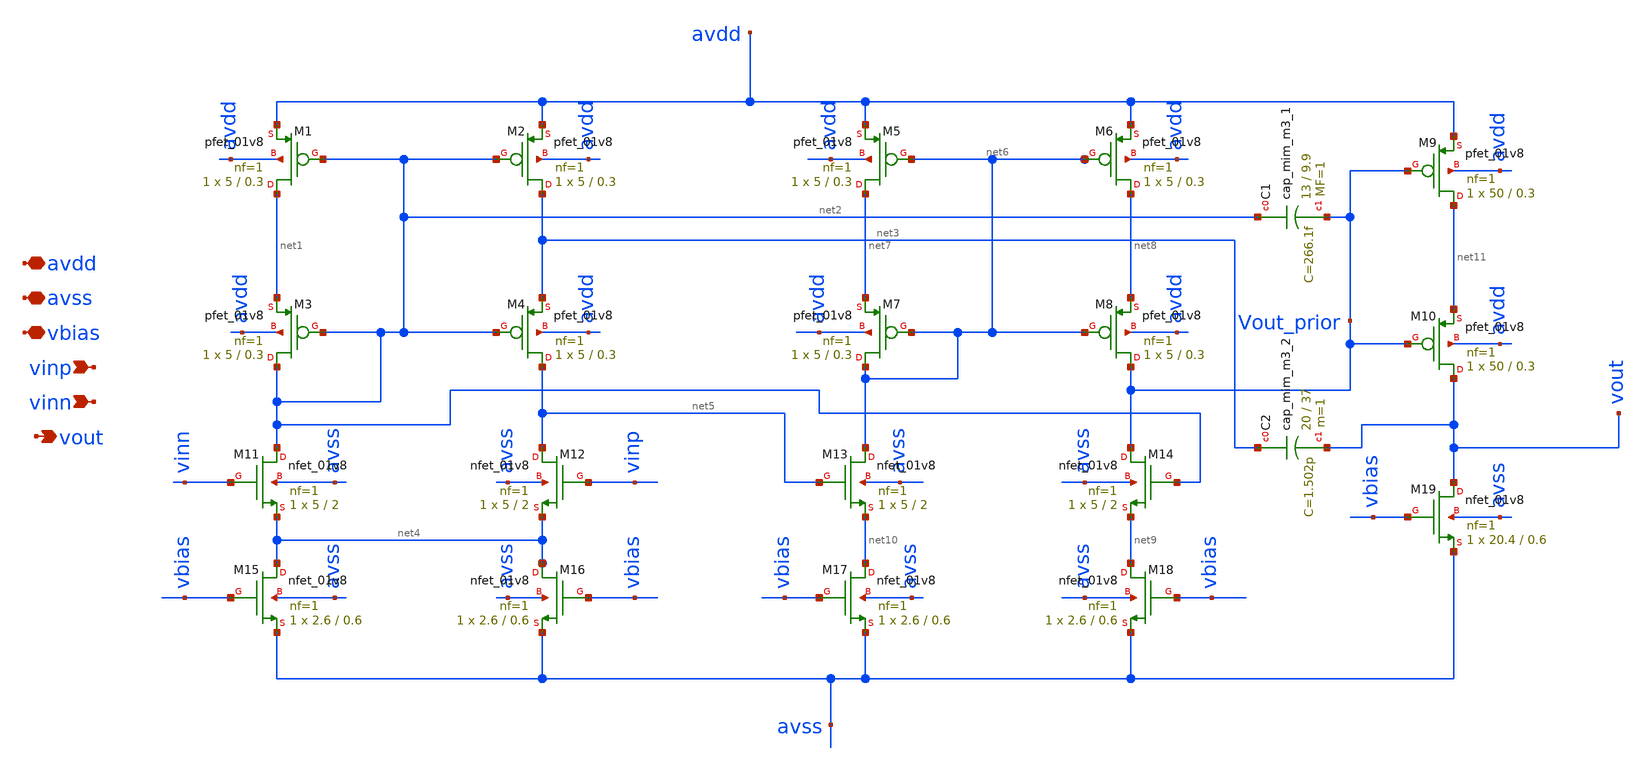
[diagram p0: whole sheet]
** sch_path: OpampHG.sch
**.subckt OpampHG avdd avss vbias vinp vinn vout
*.iopin avdd
*.iopin avss
*.iopin vbias
*.ipin vinp
*.ipin vinn
*.opin vout
XC1 net2 Vout_prior sky130_fd_pr__cap_mim_m3_1 W=13 L=9.9 MF=1 m=1
XC2 net3 vout sky130_fd_pr__cap_mim_m3_2 W=20 L=37 MF=1 m=1
XM1 net1 net2 avdd avdd sky130_fd_pr__pfet_01v8 L=0.3 W=5 nf=1 ad='int((nf+1)/2) * W/nf * 0.29' as='int((nf+2)/2) * W/nf * 0.29'
+ pd='2*int((nf+1)/2) * (W/nf + 0.29)' ps='2*int((nf+2)/2) * (W/nf + 0.29)' nrd='0.29 / W' nrs='0.29 / W'
+ sa=0 sb=0 sd=0 mult=1 m=1
XM2 net3 net2 avdd avdd sky130_fd_pr__pfet_01v8 L=0.3 W=5 nf=1 ad='int((nf+1)/2) * W/nf * 0.29' as='int((nf+2)/2) * W/nf * 0.29'
+ pd='2*int((nf+1)/2) * (W/nf + 0.29)' ps='2*int((nf+2)/2) * (W/nf + 0.29)' nrd='0.29 / W' nrs='0.29 / W'
+ sa=0 sb=0 sd=0 mult=1 m=1
XM3 net2 net2 net1 avdd sky130_fd_pr__pfet_01v8 L=0.3 W=5 nf=1 ad='int((nf+1)/2) * W/nf * 0.29' as='int((nf+2)/2) * W/nf * 0.29'
+ pd='2*int((nf+1)/2) * (W/nf + 0.29)' ps='2*int((nf+2)/2) * (W/nf + 0.29)' nrd='0.29 / W' nrs='0.29 / W'
+ sa=0 sb=0 sd=0 mult=1 m=1
XM4 net5 net2 net3 avdd sky130_fd_pr__pfet_01v8 L=0.3 W=5 nf=1 ad='int((nf+1)/2) * W/nf * 0.29' as='int((nf+2)/2) * W/nf * 0.29'
+ pd='2*int((nf+1)/2) * (W/nf + 0.29)' ps='2*int((nf+2)/2) * (W/nf + 0.29)' nrd='0.29 / W' nrs='0.29 / W'
+ sa=0 sb=0 sd=0 mult=1 m=1
XM5 net7 net6 avdd avdd sky130_fd_pr__pfet_01v8 L=0.3 W=5 nf=1 ad='int((nf+1)/2) * W/nf * 0.29' as='int((nf+2)/2) * W/nf * 0.29'
+ pd='2*int((nf+1)/2) * (W/nf + 0.29)' ps='2*int((nf+2)/2) * (W/nf + 0.29)' nrd='0.29 / W' nrs='0.29 / W'
+ sa=0 sb=0 sd=0 mult=1 m=1
XM6 net8 net6 avdd avdd sky130_fd_pr__pfet_01v8 L=0.3 W=5 nf=1 ad='int((nf+1)/2) * W/nf * 0.29' as='int((nf+2)/2) * W/nf * 0.29'
+ pd='2*int((nf+1)/2) * (W/nf + 0.29)' ps='2*int((nf+2)/2) * (W/nf + 0.29)' nrd='0.29 / W' nrs='0.29 / W'
+ sa=0 sb=0 sd=0 mult=1 m=1
XM7 net6 net6 net7 avdd sky130_fd_pr__pfet_01v8 L=0.3 W=5 nf=1 ad='int((nf+1)/2) * W/nf * 0.29' as='int((nf+2)/2) * W/nf * 0.29'
+ pd='2*int((nf+1)/2) * (W/nf + 0.29)' ps='2*int((nf+2)/2) * (W/nf + 0.29)' nrd='0.29 / W' nrs='0.29 / W'
+ sa=0 sb=0 sd=0 mult=1 m=1
XM8 Vout_prior net6 net8 avdd sky130_fd_pr__pfet_01v8 L=0.3 W=5 nf=1 ad='int((nf+1)/2) * W/nf * 0.29'
+ as='int((nf+2)/2) * W/nf * 0.29' pd='2*int((nf+1)/2) * (W/nf + 0.29)' ps='2*int((nf+2)/2) * (W/nf + 0.29)'
+ nrd='0.29 / W' nrs='0.29 / W' sa=0 sb=0 sd=0 mult=1 m=1
XM9 net11 Vout_prior avdd avdd sky130_fd_pr__pfet_01v8 L=0.3 W=50 nf=1 ad='int((nf+1)/2) * W/nf * 0.29'
+ as='int((nf+2)/2) * W/nf * 0.29' pd='2*int((nf+1)/2) * (W/nf + 0.29)' ps='2*int((nf+2)/2) * (W/nf + 0.29)'
+ nrd='0.29 / W' nrs='0.29 / W' sa=0 sb=0 sd=0 mult=1 m=1
XM10 vout Vout_prior net11 avdd sky130_fd_pr__pfet_01v8 L=0.3 W=50 nf=1 ad='int((nf+1)/2) * W/nf * 0.29'
+ as='int((nf+2)/2) * W/nf * 0.29' pd='2*int((nf+1)/2) * (W/nf + 0.29)' ps='2*int((nf+2)/2) * (W/nf + 0.29)'
+ nrd='0.29 / W' nrs='0.29 / W' sa=0 sb=0 sd=0 mult=1 m=1
XM11 net2 vinn net4 avss sky130_fd_pr__nfet_01v8 L=2 W=5 nf=1 ad='int((nf+1)/2) * W/nf * 0.29' as='int((nf+2)/2) * W/nf * 0.29'
+ pd='2*int((nf+1)/2) * (W/nf + 0.29)' ps='2*int((nf+2)/2) * (W/nf + 0.29)' nrd='0.29 / W' nrs='0.29 / W'
+ sa=0 sb=0 sd=0 mult=1 m=1
XM12 net5 vinp net4 avss sky130_fd_pr__nfet_01v8 L=2 W=5 nf=1 ad='int((nf+1)/2) * W/nf * 0.29' as='int((nf+2)/2) * W/nf * 0.29'
+ pd='2*int((nf+1)/2) * (W/nf + 0.29)' ps='2*int((nf+2)/2) * (W/nf + 0.29)' nrd='0.29 / W' nrs='0.29 / W'
+ sa=0 sb=0 sd=0 mult=1 m=1
XM13 net6 net5 net10 avss sky130_fd_pr__nfet_01v8 L=2 W=5 nf=1 ad='int((nf+1)/2) * W/nf * 0.29' as='int((nf+2)/2) * W/nf * 0.29'
+ pd='2*int((nf+1)/2) * (W/nf + 0.29)' ps='2*int((nf+2)/2) * (W/nf + 0.29)' nrd='0.29 / W' nrs='0.29 / W'
+ sa=0 sb=0 sd=0 mult=1 m=1
XM14 Vout_prior net2 net9 avss sky130_fd_pr__nfet_01v8 L=2 W=5 nf=1 ad='int((nf+1)/2) * W/nf * 0.29'
+ as='int((nf+2)/2) * W/nf * 0.29' pd='2*int((nf+1)/2) * (W/nf + 0.29)' ps='2*int((nf+2)/2) * (W/nf + 0.29)'
+ nrd='0.29 / W' nrs='0.29 / W' sa=0 sb=0 sd=0 mult=1 m=1
XM15 net4 vbias avss avss sky130_fd_pr__nfet_01v8 L=0.6 W=2.6 nf=1 ad='int((nf+1)/2) * W/nf * 0.29' as='int((nf+2)/2) * W/nf * 0.29'
+ pd='2*int((nf+1)/2) * (W/nf + 0.29)' ps='2*int((nf+2)/2) * (W/nf + 0.29)' nrd='0.29 / W' nrs='0.29 / W'
+ sa=0 sb=0 sd=0 mult=1 m=1
XM16 net4 vbias avss avss sky130_fd_pr__nfet_01v8 L=0.6 W=2.6 nf=1 ad='int((nf+1)/2) * W/nf * 0.29' as='int((nf+2)/2) * W/nf * 0.29'
+ pd='2*int((nf+1)/2) * (W/nf + 0.29)' ps='2*int((nf+2)/2) * (W/nf + 0.29)' nrd='0.29 / W' nrs='0.29 / W'
+ sa=0 sb=0 sd=0 mult=1 m=1
XM17 net10 vbias avss avss sky130_fd_pr__nfet_01v8 L=0.6 W=2.6 nf=1 ad='int((nf+1)/2) * W/nf * 0.29'
+ as='int((nf+2)/2) * W/nf * 0.29' pd='2*int((nf+1)/2) * (W/nf + 0.29)' ps='2*int((nf+2)/2) * (W/nf + 0.29)'
+ nrd='0.29 / W' nrs='0.29 / W' sa=0 sb=0 sd=0 mult=1 m=1
XM18 net9 vbias avss avss sky130_fd_pr__nfet_01v8 L=0.6 W=2.6 nf=1 ad='int((nf+1)/2) * W/nf * 0.29' as='int((nf+2)/2) * W/nf * 0.29'
+ pd='2*int((nf+1)/2) * (W/nf + 0.29)' ps='2*int((nf+2)/2) * (W/nf + 0.29)' nrd='0.29 / W' nrs='0.29 / W'
+ sa=0 sb=0 sd=0 mult=1 m=1
XM19 vout vbias avss avss sky130_fd_pr__nfet_01v8 L=0.6 W=20.4 nf=1 ad='int((nf+1)/2) * W/nf * 0.29'
+ as='int((nf+2)/2) * W/nf * 0.29' pd='2*int((nf+1)/2) * (W/nf + 0.29)' ps='2*int((nf+2)/2) * (W/nf + 0.29)'
+ nrd='0.29 / W' nrs='0.29 / W' sa=0 sb=0 sd=0 mult=1 m=1
**.ends
.end
